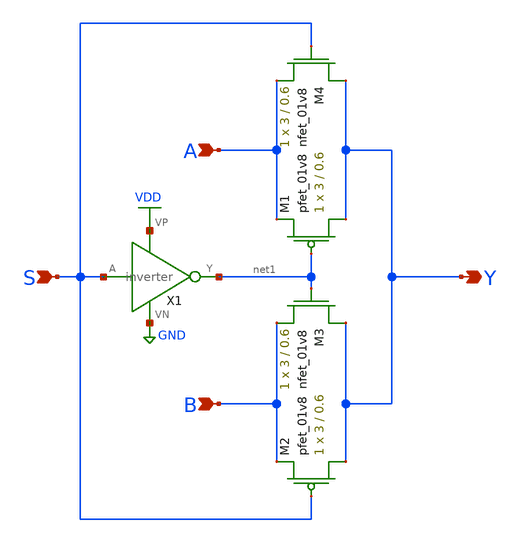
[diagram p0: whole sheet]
** sch_path: mini4/schem/mux2.sch
**.subckt mux2 Y B A S
*.opin Y
*.ipin B
*.ipin A
*.ipin S
XM1 Y net1 A VDD sky130_fd_pr__pfet_01v8 L=0.6 W=3 nf=1 ad='int((nf+1)/2) * W/nf * 0.29' as='int((nf+2)/2) * W/nf * 0.29'
+ pd='2*int((nf+1)/2) * (W/nf + 0.29)' ps='2*int((nf+2)/2) * (W/nf + 0.29)' nrd='0.29 / W' nrs='0.29 / W'
+ sa=0 sb=0 sd=0 mult=1 m=1
XM2 Y S B VDD sky130_fd_pr__pfet_01v8 L=0.6 W=3 nf=1 ad='int((nf+1)/2) * W/nf * 0.29' as='int((nf+2)/2) * W/nf * 0.29'
+ pd='2*int((nf+1)/2) * (W/nf + 0.29)' ps='2*int((nf+2)/2) * (W/nf + 0.29)' nrd='0.29 / W' nrs='0.29 / W'
+ sa=0 sb=0 sd=0 mult=1 m=1
XM3 Y net1 B GND sky130_fd_pr__nfet_01v8 L=0.6 W=3 nf=1 ad='int((nf+1)/2) * W/nf * 0.29' as='int((nf+2)/2) * W/nf * 0.29'
+ pd='2*int((nf+1)/2) * (W/nf + 0.29)' ps='2*int((nf+2)/2) * (W/nf + 0.29)' nrd='0.29 / W' nrs='0.29 / W'
+ sa=0 sb=0 sd=0 mult=1 m=1
XM4 Y S A GND sky130_fd_pr__nfet_01v8 L=0.6 W=3 nf=1 ad='int((nf+1)/2) * W/nf * 0.29' as='int((nf+2)/2) * W/nf * 0.29'
+ pd='2*int((nf+1)/2) * (W/nf + 0.29)' ps='2*int((nf+2)/2) * (W/nf + 0.29)' nrd='0.29 / W' nrs='0.29 / W'
+ sa=0 sb=0 sd=0 mult=1 m=1
X1 S net1 VDD GND inverter
**.ends
.GLOBAL VDD
.GLOBAL GND
.end
